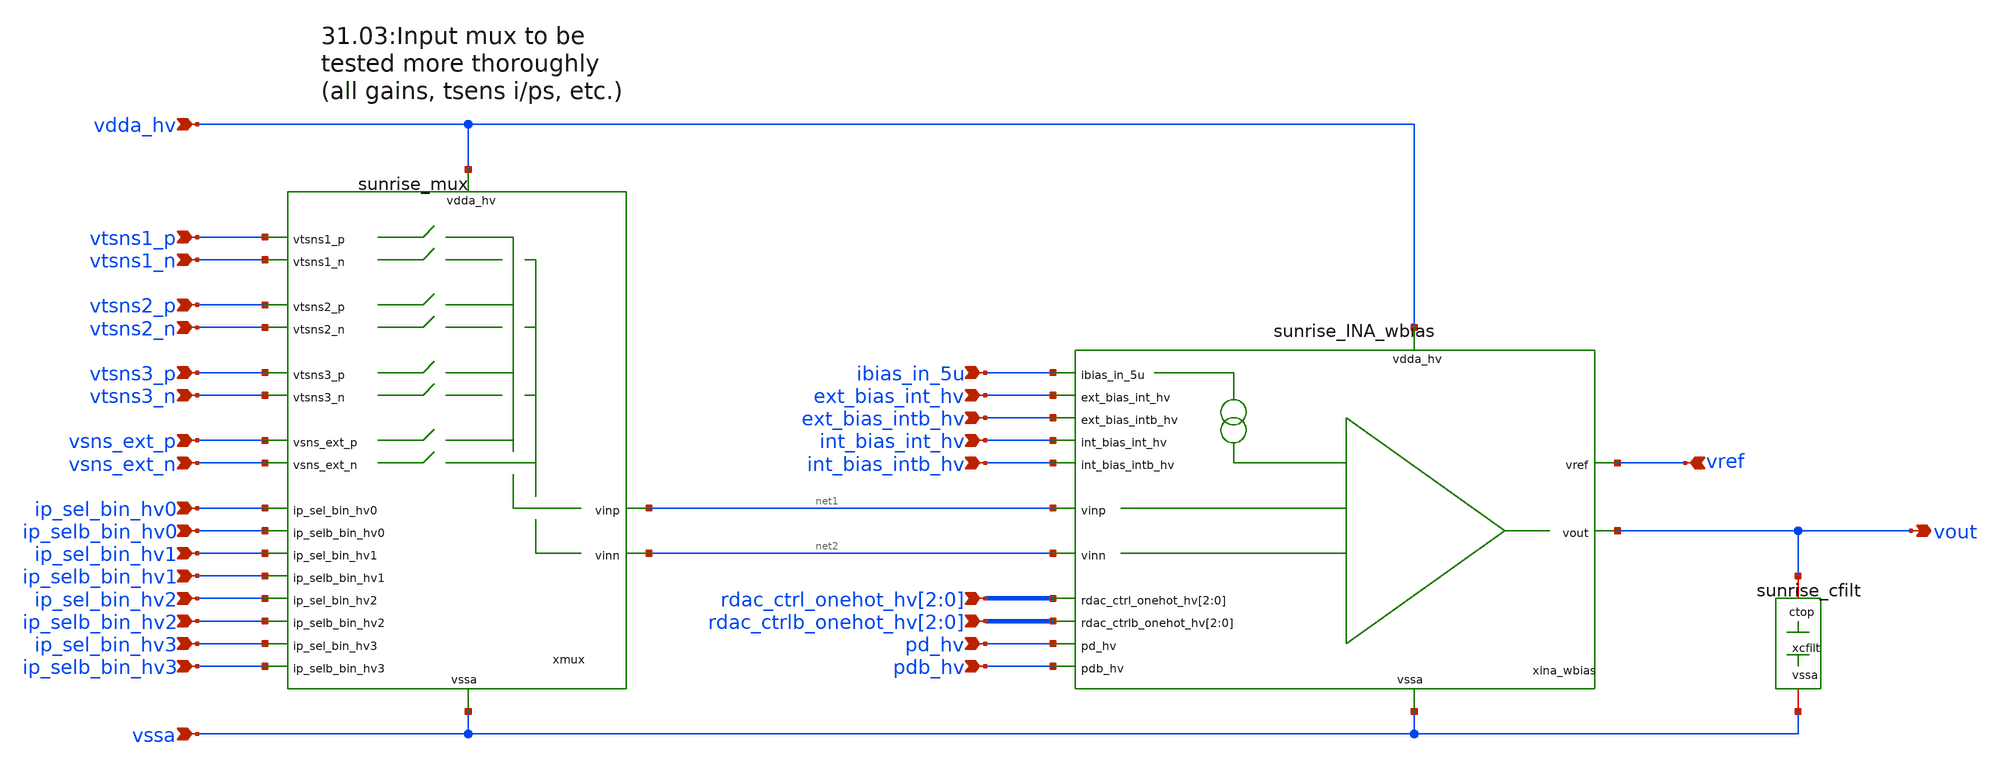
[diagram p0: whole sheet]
** sch_path: Schematics_Layout/sunrise_INA_top/sunrise_INA_top.sch
**.subckt sunrise_INA_top rdac_ctrl_onehot_hv[2],rdac_ctrl_onehot_hv[1],rdac_ctrl_onehot_hv[0]
*+ rdac_ctrlb_onehot_hv[2],rdac_ctrlb_onehot_hv[1],rdac_ctrlb_onehot_hv[0] pd_hv pdb_hv ext_bias_int_hv ext_bias_intb_hv int_bias_int_hv int_bias_intb_hv ibias_in_5u vdda_hv
*+ vssa vref vout ip_sel_bin_hv0 ip_selb_bin_hv0 ip_sel_bin_hv1 ip_selb_bin_hv1 ip_sel_bin_hv2
*+ ip_selb_bin_hv2 ip_sel_bin_hv3 ip_selb_bin_hv3 vtsns1_p vtsns1_n vtsns2_p vtsns2_n vtsns3_p vtsns3_n vsns_ext_p
*+ vsns_ext_n
*.ipin rdac_ctrl_onehot_hv[2],rdac_ctrl_onehot_hv[1],rdac_ctrl_onehot_hv[0]
*.ipin rdac_ctrlb_onehot_hv[2],rdac_ctrlb_onehot_hv[1],rdac_ctrlb_onehot_hv[0]
*.ipin pd_hv
*.ipin pdb_hv
*.ipin ext_bias_int_hv
*.ipin ext_bias_intb_hv
*.ipin int_bias_int_hv
*.ipin int_bias_intb_hv
*.ipin ibias_in_5u
*.ipin vdda_hv
*.ipin vssa
*.ipin vref
*.opin vout
*.ipin ip_sel_bin_hv0
*.ipin ip_selb_bin_hv0
*.ipin ip_sel_bin_hv1
*.ipin ip_selb_bin_hv1
*.ipin ip_sel_bin_hv2
*.ipin ip_selb_bin_hv2
*.ipin ip_sel_bin_hv3
*.ipin ip_selb_bin_hv3
*.ipin vtsns1_p
*.ipin vtsns1_n
*.ipin vtsns2_p
*.ipin vtsns2_n
*.ipin vtsns3_p
*.ipin vtsns3_n
*.ipin vsns_ext_p
*.ipin vsns_ext_n
xina_wbias vdda_hv ext_bias_int_hv ext_bias_intb_hv int_bias_int_hv int_bias_intb_hv ibias_in_5u
+ vref net1 vout net2 rdac_ctrl_onehot_hv[2] rdac_ctrl_onehot_hv[1] rdac_ctrl_onehot_hv[0]
+ rdac_ctrlb_onehot_hv[2] rdac_ctrlb_onehot_hv[1] rdac_ctrlb_onehot_hv[0] pd_hv pdb_hv vssa sunrise_INA_wbias
xcfilt vout vssa sunrise_cfilt
xmux vtsns1_p vdda_hv vssa ip_sel_bin_hv0 ip_selb_bin_hv0 ip_sel_bin_hv1 ip_selb_bin_hv1
+ ip_sel_bin_hv2 vtsns1_n ip_selb_bin_hv2 ip_sel_bin_hv3 ip_selb_bin_hv3 vtsns2_p vtsns2_n vtsns3_p vtsns3_n
+ vsns_ext_p net1 net2 vsns_ext_n sunrise_mux
**.ends
.end
